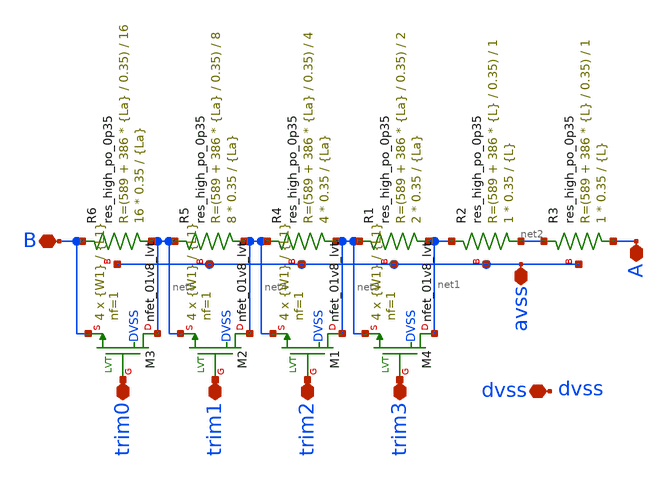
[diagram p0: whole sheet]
** sch_path: xschem/Resistor50k_1.sch
**.subckt Resistor50k_1 A B avss dvss trim3 trim2 trim1 trim0
*.iopin A
*.iopin B
*.iopin avss
*.iopin dvss
*.iopin trim3
*.iopin trim2
*.iopin trim1
*.iopin trim0
XR2 net2 net1 avss sky130_fd_pr__res_high_po_0p35 L={L} mult=1 m=1
XR3 A net2 avss sky130_fd_pr__res_high_po_0p35 L={L} mult=1 m=1
XR1 net1 net3 avss sky130_fd_pr__res_high_po_0p35 L={La} mult=2 m=2
XR4 net3 net4 avss sky130_fd_pr__res_high_po_0p35 L={La} mult=4 m=4
XR5 net4 net5 avss sky130_fd_pr__res_high_po_0p35 L={La} mult=8 m=8
XR6 net5 B avss sky130_fd_pr__res_high_po_0p35 L={La} mult=16 m=16
XM4 net1 trim3 net3 DVSS sky130_fd_pr__nfet_01v8_lvt L={L1} W={W1} nf=1 ad='int((nf+1)/2) * W/nf * 0.29'
+ as='int((nf+2)/2) * W/nf * 0.29' pd='2*int((nf+1)/2) * (W/nf + 0.29)' ps='2*int((nf+2)/2) * (W/nf + 0.29)'
+ nrd='0.29 / W' nrs='0.29 / W' sa=0 sb=0 sd=0 mult=4 m=4
XM1 net3 trim2 net4 DVSS sky130_fd_pr__nfet_01v8_lvt L={L1} W={W1} nf=1 ad='int((nf+1)/2) * W/nf * 0.29'
+ as='int((nf+2)/2) * W/nf * 0.29' pd='2*int((nf+1)/2) * (W/nf + 0.29)' ps='2*int((nf+2)/2) * (W/nf + 0.29)'
+ nrd='0.29 / W' nrs='0.29 / W' sa=0 sb=0 sd=0 mult=4 m=4
XM2 net4 trim1 net5 DVSS sky130_fd_pr__nfet_01v8_lvt L={L1} W={W1} nf=1 ad='int((nf+1)/2) * W/nf * 0.29'
+ as='int((nf+2)/2) * W/nf * 0.29' pd='2*int((nf+1)/2) * (W/nf + 0.29)' ps='2*int((nf+2)/2) * (W/nf + 0.29)'
+ nrd='0.29 / W' nrs='0.29 / W' sa=0 sb=0 sd=0 mult=4 m=4
XM3 net5 trim0 B DVSS sky130_fd_pr__nfet_01v8_lvt L={L1} W={W1} nf=1 ad='int((nf+1)/2) * W/nf * 0.29'
+ as='int((nf+2)/2) * W/nf * 0.29' pd='2*int((nf+1)/2) * (W/nf + 0.29)' ps='2*int((nf+2)/2) * (W/nf + 0.29)'
+ nrd='0.29 / W' nrs='0.29 / W' sa=0 sb=0 sd=0 mult=4 m=4
**** begin user architecture code


.param L=17
.param La=8.8
.param L1=1
.param W1=4


**** end user architecture code
**.ends
.end
